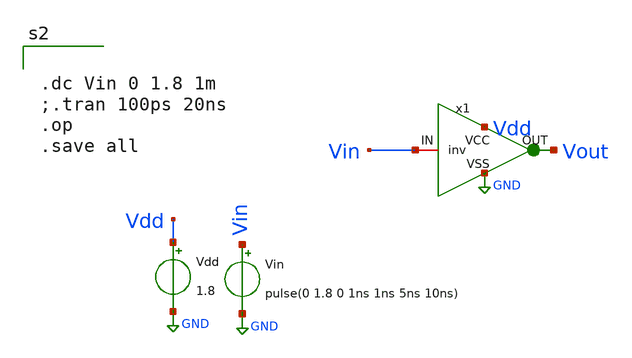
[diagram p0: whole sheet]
** sch_path: inv_test.sch
**.subckt inv_test
Vdd Vdd GND 1.8
Vin Vin GND pulse(0 1.8 0 1ns 1ns 5ns 10ns)
x1 Vdd Vin Vout GND inv
**** begin user architecture code


.dc Vin 0 1.8 1m
;.tran 100ps 20ns
.op
.save all



** opencircuitdesign pdks install
.lib $::SKYWATER_MODELS/sky130.lib.spice tt

**** end user architecture code
**.ends

* expanding   symbol:  inv.sym # of pins=4
** sym_path: inv.sym
** sch_path: inv.sch
.subckt inv VCC IN OUT VSS
*.iopin VCC
*.iopin IN
*.iopin OUT
*.iopin VSS
XM1 OUT IN VSS VSS sky130_fd_pr__nfet_01v8 L=0.15 W=0.5 nf=1 ad='int((nf+1)/2) * W/nf * 0.29' as='int((nf+2)/2) * W/nf * 0.29'
+ pd='2*int((nf+1)/2) * (W/nf + 0.29)' ps='2*int((nf+2)/2) * (W/nf + 0.29)' nrd='0.29 / W' nrs='0.29 / W'
+ sa=0 sb=0 sd=0 mult=1 m=1
XM2 OUT IN VCC VCC sky130_fd_pr__pfet_01v8 L=0.15 W=1.05 nf=1 ad='int((nf+1)/2) * W/nf * 0.29' as='int((nf+2)/2) * W/nf * 0.29'
+ pd='2*int((nf+1)/2) * (W/nf + 0.29)' ps='2*int((nf+2)/2) * (W/nf + 0.29)' nrd='0.29 / W' nrs='0.29 / W'
+ sa=0 sb=0 sd=0 mult=1 m=1
.ends

.GLOBAL GND
.end
